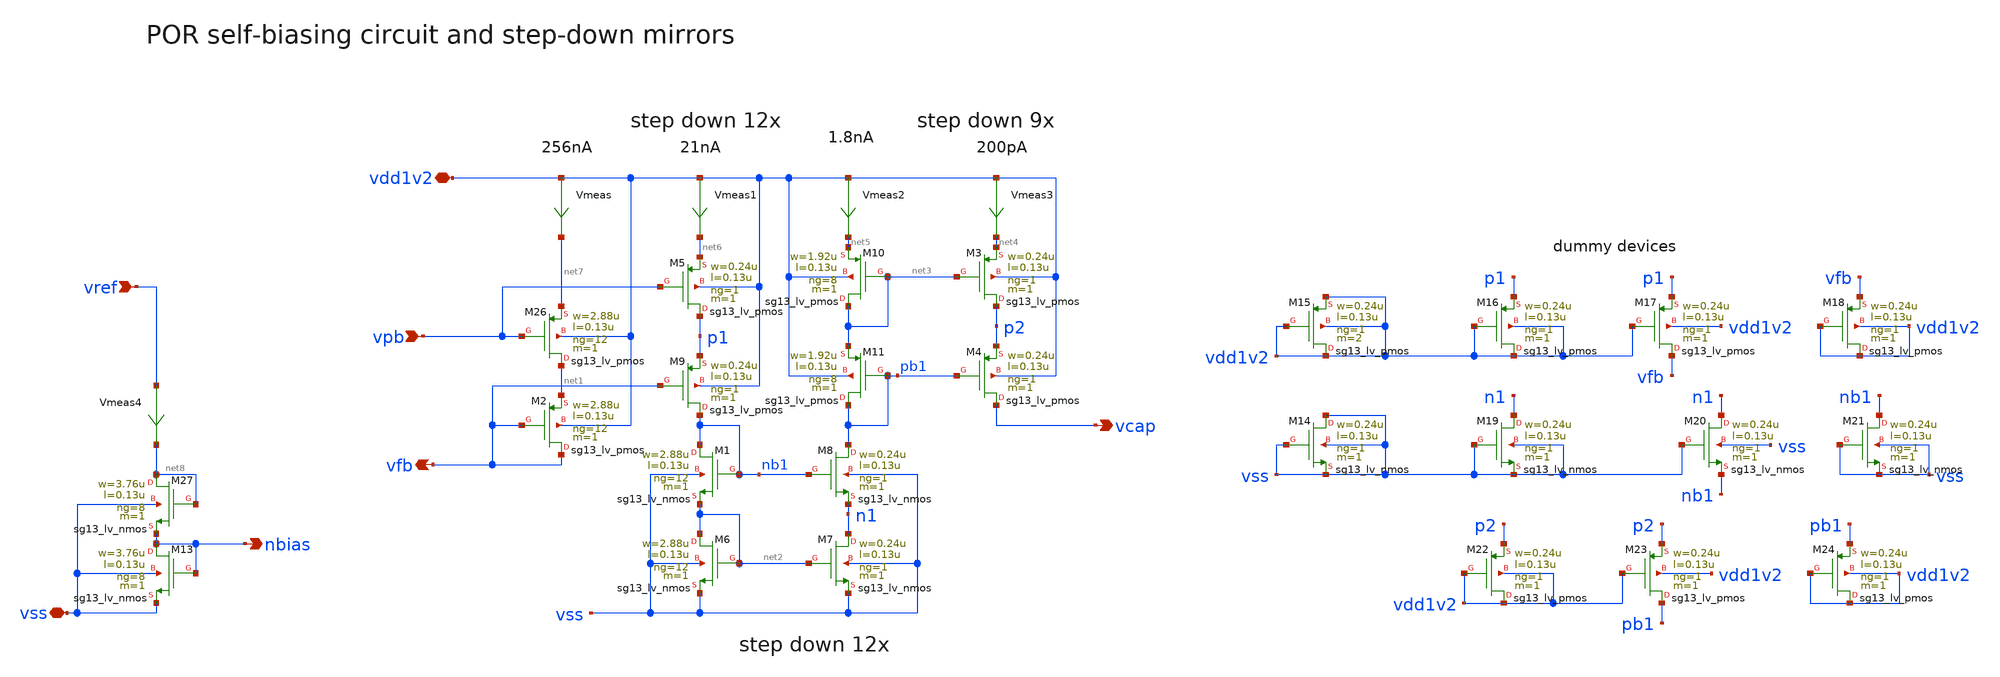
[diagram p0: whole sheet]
** sch_path: xschem/por_stepdown.sch
**.subckt por_stepdown vdd1v2 vss nbias vref vpb vfb vcap
*.iopin vdd1v2
*.iopin vss
*.opin nbias
*.ipin vref
*.ipin vpb
*.opin vfb
*.opin vcap
Vmeas vdd1v2 net7 0
.save i(vmeas)
Vmeas1 vdd1v2 net6 0
.save i(vmeas1)
Vmeas2 vdd1v2 net5 0
.save i(vmeas2)
Vmeas3 vdd1v2 net4 0
.save i(vmeas3)
Vmeas4 vref net8 0
.save i(vmeas4)
XM26 net1 vpb net7 vdd1v2 sg13_lv_pmos w=2.88u l=0.13u ng=12 m=1 mm_ok=1
XM27 net8 net8 nbias vss sg13_lv_nmos w=3.76u l=0.13u ng=8 m=1 mm_ok=1
XM13 nbias nbias vss vss sg13_lv_nmos w=3.76u l=0.13u ng=8 m=1 mm_ok=1
XM1 nb1 nb1 net2 vss sg13_lv_nmos w=2.88u l=0.13u ng=12 m=1 mm_ok=1
XM6 net2 net2 vss vss sg13_lv_nmos w=2.88u l=0.13u ng=12 m=1 mm_ok=1
XM7 n1 net2 vss vss sg13_lv_nmos w=0.24u l=0.13u ng=1 m=1 mm_ok=1
XM8 pb1 nb1 n1 vss sg13_lv_nmos w=0.24u l=0.13u ng=1 m=1 mm_ok=1
XM14 vss vss vss vss sg13_lv_nmos w=0.24u l=0.13u ng=1 m=1 mm_ok=1
XM19 n1 vss vss vss sg13_lv_nmos w=0.24u l=0.13u ng=1 m=1 mm_ok=1
XM20 n1 vss nb1 vss sg13_lv_nmos w=0.24u l=0.13u ng=1 m=1 mm_ok=1
XM21 nb1 vss vss vss sg13_lv_nmos w=0.24u l=0.13u ng=1 m=1 mm_ok=1
XM15 vdd1v2 vdd1v2 vdd1v2 vdd1v2 sg13_lv_pmos w=0.24u l=0.13u ng=1 m=2 mm_ok=1
XM16 vdd1v2 vdd1v2 p1 vdd1v2 sg13_lv_pmos w=0.24u l=0.13u ng=1 m=1 mm_ok=1
XM17 vfb vdd1v2 p1 vdd1v2 sg13_lv_pmos w=0.24u l=0.13u ng=1 m=1 mm_ok=1
XM18 vdd1v2 vdd1v2 vfb vdd1v2 sg13_lv_pmos w=0.24u l=0.13u ng=1 m=1 mm_ok=1
XM22 vdd1v2 vdd1v2 p2 vdd1v2 sg13_lv_pmos w=0.24u l=0.13u ng=1 m=1 mm_ok=1
XM23 pb1 vdd1v2 p2 vdd1v2 sg13_lv_pmos w=0.24u l=0.13u ng=1 m=1 mm_ok=1
XM24 vdd1v2 vdd1v2 pb1 vdd1v2 sg13_lv_pmos w=0.24u l=0.13u ng=1 m=1 mm_ok=1
XM2 vfb vfb net1 vdd1v2 sg13_lv_pmos w=2.88u l=0.13u ng=12 m=1 mm_ok=1
XM3 p2 net3 net4 vdd1v2 sg13_lv_pmos w=0.24u l=0.13u ng=1 m=1 mm_ok=1
XM4 vcap pb1 p2 vdd1v2 sg13_lv_pmos w=0.24u l=0.13u ng=1 m=1 mm_ok=1
XM5 p1 vpb net6 vdd1v2 sg13_lv_pmos w=0.24u l=0.13u ng=1 m=1 mm_ok=1
XM9 nb1 vfb p1 vdd1v2 sg13_lv_pmos w=0.24u l=0.13u ng=1 m=1 mm_ok=1
XM10 net3 net3 net5 vdd1v2 sg13_lv_pmos w=1.92u l=0.13u ng=8 m=1 mm_ok=1
XM11 pb1 pb1 net3 vdd1v2 sg13_lv_pmos w=1.92u l=0.13u ng=8 m=1 mm_ok=1
**.ends
.end
